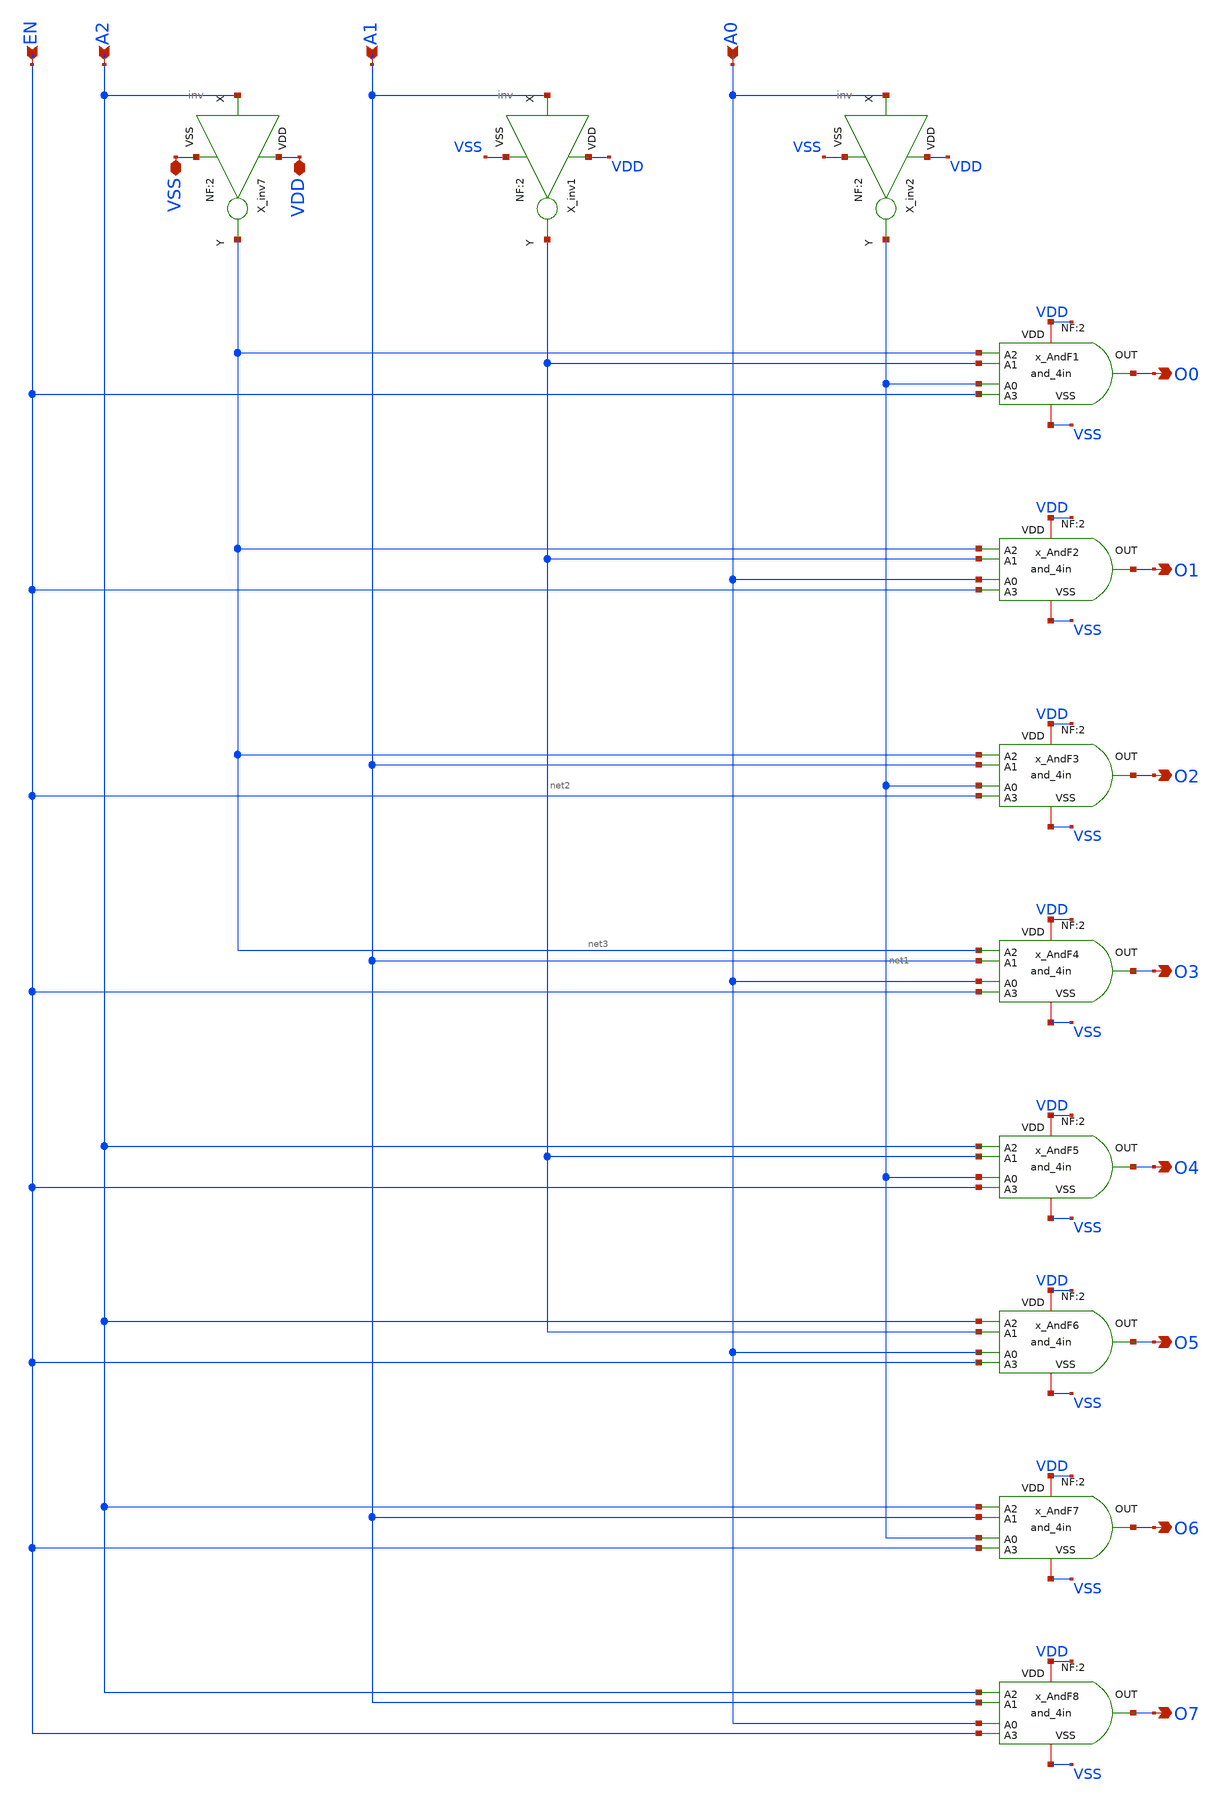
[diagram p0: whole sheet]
** sch_path: xschem_lib/sylee21/dec_3to8.sch
**.subckt dec_3to8 A2 A1 A0 VDD VSS O0 O1 O2 O3 O4 O5 O6 O7 EN
*.ipin A2
*.ipin A1
*.ipin A0
*.iopin VDD
*.iopin VSS
*.opin O0
*.opin O1
*.opin O2
*.opin O3
*.opin O4
*.opin O5
*.opin O6
*.opin O7
*.ipin EN
X_inv7 A2 VDD VSS net3 inv NF=2
X_inv1 A1 VDD VSS net2 inv NF=2
X_inv2 A0 VDD VSS net1 inv NF=2
x_AndF1 net3 net2 O0 VDD VSS net1 EN and_4in NF=2
x_AndF2 net3 net2 O1 VDD VSS A0 EN and_4in NF=2
x_AndF3 net3 A1 O2 VDD VSS net1 EN and_4in NF=2
x_AndF4 net3 A1 O3 VDD VSS A0 EN and_4in NF=2
x_AndF5 A2 net2 O4 VDD VSS net1 EN and_4in NF=2
x_AndF6 A2 net2 O5 VDD VSS A0 EN and_4in NF=2
x_AndF7 A2 A1 O6 VDD VSS net1 EN and_4in NF=2
x_AndF8 A2 A1 O7 VDD VSS A0 EN and_4in NF=2
**.ends
.end
